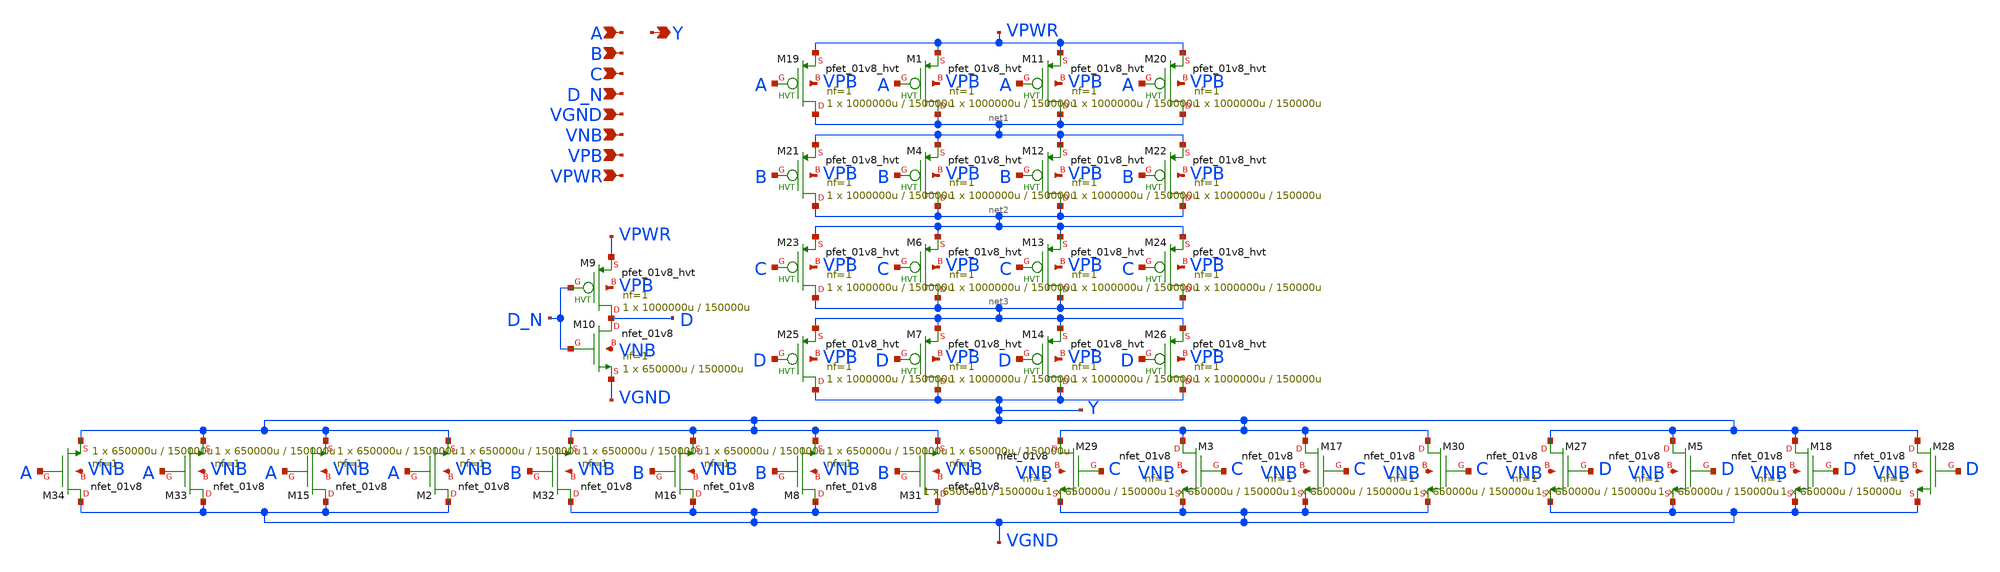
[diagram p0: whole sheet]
** sch_path: schematics/nor4b/sky130_fd_sc_hd__nor4b_4.sch
**.subckt sky130_fd_sc_hd__nor4b_4 A B C D_N VGND VNB VPB VPWR Y
*.ipin A
*.ipin B
*.ipin C
*.ipin D_N
*.ipin VGND
*.ipin VNB
*.ipin VPB
*.ipin VPWR
*.opin Y
XM1 net1 A VPWR VPB sky130_fd_pr__pfet_01v8_hvt L=150000u W=1000000u nf=1 ad='int((1 + 1)/2) * 1000000u / 1 * 0.29'
+ as='int((1 + 2)/2) * 1000000u / 1 * 0.29' pd='2*int((1 + 1)/2) * (1000000u / 1 + 0.29)' ps='2*int((1 + 2)/2) * (1000000u / 1 + 0.29)'
+ nrd='0.29 / 1000000u ' nrs='0.29 / 1000000u ' sa=0 sb=0 sd=0 mult=1 m=1
XM2 VGND A Y VNB sky130_fd_pr__nfet_01v8 L=150000u W=650000u nf=1 ad='int((1 + 1)/2) * 650000u / 1 * 0.29'
+ as='int((1 + 2)/2) * 650000u / 1 * 0.29' pd='2*int((1 + 1)/2) * (650000u / 1 + 0.29)' ps='2*int((1 + 2)/2) * (650000u / 1 + 0.29)'
+ nrd='0.29 / 650000u ' nrs='0.29 / 650000u ' sa=0 sb=0 sd=0 mult=1 m=1
XM4 net2 B net1 VPB sky130_fd_pr__pfet_01v8_hvt L=150000u W=1000000u nf=1 ad='int((1 + 1)/2) * 1000000u / 1 * 0.29'
+ as='int((1 + 2)/2) * 1000000u / 1 * 0.29' pd='2*int((1 + 1)/2) * (1000000u / 1 + 0.29)' ps='2*int((1 + 2)/2) * (1000000u / 1 + 0.29)'
+ nrd='0.29 / 1000000u ' nrs='0.29 / 1000000u ' sa=0 sb=0 sd=0 mult=1 m=1
XM3 Y C VGND VNB sky130_fd_pr__nfet_01v8 L=150000u W=650000u nf=1 ad='int((1 + 1)/2) * 650000u / 1 * 0.29'
+ as='int((1 + 2)/2) * 650000u / 1 * 0.29' pd='2*int((1 + 1)/2) * (650000u / 1 + 0.29)' ps='2*int((1 + 2)/2) * (650000u / 1 + 0.29)'
+ nrd='0.29 / 650000u ' nrs='0.29 / 650000u ' sa=0 sb=0 sd=0 mult=1 m=1
XM5 Y D VGND VNB sky130_fd_pr__nfet_01v8 L=150000u W=650000u nf=1 ad='int((1 + 1)/2) * 650000u / 1 * 0.29'
+ as='int((1 + 2)/2) * 650000u / 1 * 0.29' pd='2*int((1 + 1)/2) * (650000u / 1 + 0.29)' ps='2*int((1 + 2)/2) * (650000u / 1 + 0.29)'
+ nrd='0.29 / 650000u ' nrs='0.29 / 650000u ' sa=0 sb=0 sd=0 mult=1 m=1
XM6 net3 C net2 VPB sky130_fd_pr__pfet_01v8_hvt L=150000u W=1000000u nf=1 ad='int((1 + 1)/2) * 1000000u / 1 * 0.29'
+ as='int((1 + 2)/2) * 1000000u / 1 * 0.29' pd='2*int((1 + 1)/2) * (1000000u / 1 + 0.29)' ps='2*int((1 + 2)/2) * (1000000u / 1 + 0.29)'
+ nrd='0.29 / 1000000u ' nrs='0.29 / 1000000u ' sa=0 sb=0 sd=0 mult=1 m=1
XM7 Y D net3 VPB sky130_fd_pr__pfet_01v8_hvt L=150000u W=1000000u nf=1 ad='int((1 + 1)/2) * 1000000u / 1 * 0.29'
+ as='int((1 + 2)/2) * 1000000u / 1 * 0.29' pd='2*int((1 + 1)/2) * (1000000u / 1 + 0.29)' ps='2*int((1 + 2)/2) * (1000000u / 1 + 0.29)'
+ nrd='0.29 / 1000000u ' nrs='0.29 / 1000000u ' sa=0 sb=0 sd=0 mult=1 m=1
XM8 VGND B Y VNB sky130_fd_pr__nfet_01v8 L=150000u W=650000u nf=1 ad='int((1 + 1)/2) * 650000u / 1 * 0.29'
+ as='int((1 + 2)/2) * 650000u / 1 * 0.29' pd='2*int((1 + 1)/2) * (650000u / 1 + 0.29)' ps='2*int((1 + 2)/2) * (650000u / 1 + 0.29)'
+ nrd='0.29 / 650000u ' nrs='0.29 / 650000u ' sa=0 sb=0 sd=0 mult=1 m=1
XM9 D D_N VPWR VPB sky130_fd_pr__pfet_01v8_hvt L=150000u W=1000000u nf=1 ad='int((1 + 1)/2) * 1000000u / 1 * 0.29'
+ as='int((1 + 2)/2) * 1000000u / 1 * 0.29' pd='2*int((1 + 1)/2) * (1000000u / 1 + 0.29)' ps='2*int((1 + 2)/2) * (1000000u / 1 + 0.29)'
+ nrd='0.29 / 1000000u ' nrs='0.29 / 1000000u ' sa=0 sb=0 sd=0 mult=1 m=1
XM10 D D_N VGND VNB sky130_fd_pr__nfet_01v8 L=150000u W=650000u nf=1 ad='int((1 + 1)/2) * 650000u / 1 * 0.29'
+ as='int((1 + 2)/2) * 650000u / 1 * 0.29' pd='2*int((1 + 1)/2) * (650000u / 1 + 0.29)' ps='2*int((1 + 2)/2) * (650000u / 1 + 0.29)'
+ nrd='0.29 / 650000u ' nrs='0.29 / 650000u ' sa=0 sb=0 sd=0 mult=1 m=1
XM11 net1 A VPWR VPB sky130_fd_pr__pfet_01v8_hvt L=150000u W=1000000u nf=1 ad='int((1 + 1)/2) * 1000000u / 1 * 0.29'
+ as='int((1 + 2)/2) * 1000000u / 1 * 0.29' pd='2*int((1 + 1)/2) * (1000000u / 1 + 0.29)' ps='2*int((1 + 2)/2) * (1000000u / 1 + 0.29)'
+ nrd='0.29 / 1000000u ' nrs='0.29 / 1000000u ' sa=0 sb=0 sd=0 mult=1 m=1
XM12 net2 B net1 VPB sky130_fd_pr__pfet_01v8_hvt L=150000u W=1000000u nf=1 ad='int((1 + 1)/2) * 1000000u / 1 * 0.29'
+ as='int((1 + 2)/2) * 1000000u / 1 * 0.29' pd='2*int((1 + 1)/2) * (1000000u / 1 + 0.29)' ps='2*int((1 + 2)/2) * (1000000u / 1 + 0.29)'
+ nrd='0.29 / 1000000u ' nrs='0.29 / 1000000u ' sa=0 sb=0 sd=0 mult=1 m=1
XM13 net3 C net2 VPB sky130_fd_pr__pfet_01v8_hvt L=150000u W=1000000u nf=1 ad='int((1 + 1)/2) * 1000000u / 1 * 0.29'
+ as='int((1 + 2)/2) * 1000000u / 1 * 0.29' pd='2*int((1 + 1)/2) * (1000000u / 1 + 0.29)' ps='2*int((1 + 2)/2) * (1000000u / 1 + 0.29)'
+ nrd='0.29 / 1000000u ' nrs='0.29 / 1000000u ' sa=0 sb=0 sd=0 mult=1 m=1
XM14 Y D net3 VPB sky130_fd_pr__pfet_01v8_hvt L=150000u W=1000000u nf=1 ad='int((1 + 1)/2) * 1000000u / 1 * 0.29'
+ as='int((1 + 2)/2) * 1000000u / 1 * 0.29' pd='2*int((1 + 1)/2) * (1000000u / 1 + 0.29)' ps='2*int((1 + 2)/2) * (1000000u / 1 + 0.29)'
+ nrd='0.29 / 1000000u ' nrs='0.29 / 1000000u ' sa=0 sb=0 sd=0 mult=1 m=1
XM15 VGND A Y VNB sky130_fd_pr__nfet_01v8 L=150000u W=650000u nf=1 ad='int((1 + 1)/2) * 650000u / 1 * 0.29'
+ as='int((1 + 2)/2) * 650000u / 1 * 0.29' pd='2*int((1 + 1)/2) * (650000u / 1 + 0.29)' ps='2*int((1 + 2)/2) * (650000u / 1 + 0.29)'
+ nrd='0.29 / 650000u ' nrs='0.29 / 650000u ' sa=0 sb=0 sd=0 mult=1 m=1
XM16 VGND B Y VNB sky130_fd_pr__nfet_01v8 L=150000u W=650000u nf=1 ad='int((1 + 1)/2) * 650000u / 1 * 0.29'
+ as='int((1 + 2)/2) * 650000u / 1 * 0.29' pd='2*int((1 + 1)/2) * (650000u / 1 + 0.29)' ps='2*int((1 + 2)/2) * (650000u / 1 + 0.29)'
+ nrd='0.29 / 650000u ' nrs='0.29 / 650000u ' sa=0 sb=0 sd=0 mult=1 m=1
XM17 Y C VGND VNB sky130_fd_pr__nfet_01v8 L=150000u W=650000u nf=1 ad='int((1 + 1)/2) * 650000u / 1 * 0.29'
+ as='int((1 + 2)/2) * 650000u / 1 * 0.29' pd='2*int((1 + 1)/2) * (650000u / 1 + 0.29)' ps='2*int((1 + 2)/2) * (650000u / 1 + 0.29)'
+ nrd='0.29 / 650000u ' nrs='0.29 / 650000u ' sa=0 sb=0 sd=0 mult=1 m=1
XM18 Y D VGND VNB sky130_fd_pr__nfet_01v8 L=150000u W=650000u nf=1 ad='int((1 + 1)/2) * 650000u / 1 * 0.29'
+ as='int((1 + 2)/2) * 650000u / 1 * 0.29' pd='2*int((1 + 1)/2) * (650000u / 1 + 0.29)' ps='2*int((1 + 2)/2) * (650000u / 1 + 0.29)'
+ nrd='0.29 / 650000u ' nrs='0.29 / 650000u ' sa=0 sb=0 sd=0 mult=1 m=1
XM19 net1 A VPWR VPB sky130_fd_pr__pfet_01v8_hvt L=150000u W=1000000u nf=1 ad='int((1 + 1)/2) * 1000000u / 1 * 0.29'
+ as='int((1 + 2)/2) * 1000000u / 1 * 0.29' pd='2*int((1 + 1)/2) * (1000000u / 1 + 0.29)' ps='2*int((1 + 2)/2) * (1000000u / 1 + 0.29)'
+ nrd='0.29 / 1000000u ' nrs='0.29 / 1000000u ' sa=0 sb=0 sd=0 mult=1 m=1
XM20 net1 A VPWR VPB sky130_fd_pr__pfet_01v8_hvt L=150000u W=1000000u nf=1 ad='int((1 + 1)/2) * 1000000u / 1 * 0.29'
+ as='int((1 + 2)/2) * 1000000u / 1 * 0.29' pd='2*int((1 + 1)/2) * (1000000u / 1 + 0.29)' ps='2*int((1 + 2)/2) * (1000000u / 1 + 0.29)'
+ nrd='0.29 / 1000000u ' nrs='0.29 / 1000000u ' sa=0 sb=0 sd=0 mult=1 m=1
XM21 net2 B net1 VPB sky130_fd_pr__pfet_01v8_hvt L=150000u W=1000000u nf=1 ad='int((1 + 1)/2) * 1000000u / 1 * 0.29'
+ as='int((1 + 2)/2) * 1000000u / 1 * 0.29' pd='2*int((1 + 1)/2) * (1000000u / 1 + 0.29)' ps='2*int((1 + 2)/2) * (1000000u / 1 + 0.29)'
+ nrd='0.29 / 1000000u ' nrs='0.29 / 1000000u ' sa=0 sb=0 sd=0 mult=1 m=1
XM22 net2 B net1 VPB sky130_fd_pr__pfet_01v8_hvt L=150000u W=1000000u nf=1 ad='int((1 + 1)/2) * 1000000u / 1 * 0.29'
+ as='int((1 + 2)/2) * 1000000u / 1 * 0.29' pd='2*int((1 + 1)/2) * (1000000u / 1 + 0.29)' ps='2*int((1 + 2)/2) * (1000000u / 1 + 0.29)'
+ nrd='0.29 / 1000000u ' nrs='0.29 / 1000000u ' sa=0 sb=0 sd=0 mult=1 m=1
XM23 net3 C net2 VPB sky130_fd_pr__pfet_01v8_hvt L=150000u W=1000000u nf=1 ad='int((1 + 1)/2) * 1000000u / 1 * 0.29'
+ as='int((1 + 2)/2) * 1000000u / 1 * 0.29' pd='2*int((1 + 1)/2) * (1000000u / 1 + 0.29)' ps='2*int((1 + 2)/2) * (1000000u / 1 + 0.29)'
+ nrd='0.29 / 1000000u ' nrs='0.29 / 1000000u ' sa=0 sb=0 sd=0 mult=1 m=1
XM24 net3 C net2 VPB sky130_fd_pr__pfet_01v8_hvt L=150000u W=1000000u nf=1 ad='int((1 + 1)/2) * 1000000u / 1 * 0.29'
+ as='int((1 + 2)/2) * 1000000u / 1 * 0.29' pd='2*int((1 + 1)/2) * (1000000u / 1 + 0.29)' ps='2*int((1 + 2)/2) * (1000000u / 1 + 0.29)'
+ nrd='0.29 / 1000000u ' nrs='0.29 / 1000000u ' sa=0 sb=0 sd=0 mult=1 m=1
XM25 Y D net3 VPB sky130_fd_pr__pfet_01v8_hvt L=150000u W=1000000u nf=1 ad='int((1 + 1)/2) * 1000000u / 1 * 0.29'
+ as='int((1 + 2)/2) * 1000000u / 1 * 0.29' pd='2*int((1 + 1)/2) * (1000000u / 1 + 0.29)' ps='2*int((1 + 2)/2) * (1000000u / 1 + 0.29)'
+ nrd='0.29 / 1000000u ' nrs='0.29 / 1000000u ' sa=0 sb=0 sd=0 mult=1 m=1
XM26 Y D net3 VPB sky130_fd_pr__pfet_01v8_hvt L=150000u W=1000000u nf=1 ad='int((1 + 1)/2) * 1000000u / 1 * 0.29'
+ as='int((1 + 2)/2) * 1000000u / 1 * 0.29' pd='2*int((1 + 1)/2) * (1000000u / 1 + 0.29)' ps='2*int((1 + 2)/2) * (1000000u / 1 + 0.29)'
+ nrd='0.29 / 1000000u ' nrs='0.29 / 1000000u ' sa=0 sb=0 sd=0 mult=1 m=1
XM27 Y D VGND VNB sky130_fd_pr__nfet_01v8 L=150000u W=650000u nf=1 ad='int((1 + 1)/2) * 650000u / 1 * 0.29'
+ as='int((1 + 2)/2) * 650000u / 1 * 0.29' pd='2*int((1 + 1)/2) * (650000u / 1 + 0.29)' ps='2*int((1 + 2)/2) * (650000u / 1 + 0.29)'
+ nrd='0.29 / 650000u ' nrs='0.29 / 650000u ' sa=0 sb=0 sd=0 mult=1 m=1
XM28 Y D VGND VNB sky130_fd_pr__nfet_01v8 L=150000u W=650000u nf=1 ad='int((1 + 1)/2) * 650000u / 1 * 0.29'
+ as='int((1 + 2)/2) * 650000u / 1 * 0.29' pd='2*int((1 + 1)/2) * (650000u / 1 + 0.29)' ps='2*int((1 + 2)/2) * (650000u / 1 + 0.29)'
+ nrd='0.29 / 650000u ' nrs='0.29 / 650000u ' sa=0 sb=0 sd=0 mult=1 m=1
XM29 Y C VGND VNB sky130_fd_pr__nfet_01v8 L=150000u W=650000u nf=1 ad='int((1 + 1)/2) * 650000u / 1 * 0.29'
+ as='int((1 + 2)/2) * 650000u / 1 * 0.29' pd='2*int((1 + 1)/2) * (650000u / 1 + 0.29)' ps='2*int((1 + 2)/2) * (650000u / 1 + 0.29)'
+ nrd='0.29 / 650000u ' nrs='0.29 / 650000u ' sa=0 sb=0 sd=0 mult=1 m=1
XM30 Y C VGND VNB sky130_fd_pr__nfet_01v8 L=150000u W=650000u nf=1 ad='int((1 + 1)/2) * 650000u / 1 * 0.29'
+ as='int((1 + 2)/2) * 650000u / 1 * 0.29' pd='2*int((1 + 1)/2) * (650000u / 1 + 0.29)' ps='2*int((1 + 2)/2) * (650000u / 1 + 0.29)'
+ nrd='0.29 / 650000u ' nrs='0.29 / 650000u ' sa=0 sb=0 sd=0 mult=1 m=1
XM31 VGND B Y VNB sky130_fd_pr__nfet_01v8 L=150000u W=650000u nf=1 ad='int((1 + 1)/2) * 650000u / 1 * 0.29'
+ as='int((1 + 2)/2) * 650000u / 1 * 0.29' pd='2*int((1 + 1)/2) * (650000u / 1 + 0.29)' ps='2*int((1 + 2)/2) * (650000u / 1 + 0.29)'
+ nrd='0.29 / 650000u ' nrs='0.29 / 650000u ' sa=0 sb=0 sd=0 mult=1 m=1
XM32 VGND B Y VNB sky130_fd_pr__nfet_01v8 L=150000u W=650000u nf=1 ad='int((1 + 1)/2) * 650000u / 1 * 0.29'
+ as='int((1 + 2)/2) * 650000u / 1 * 0.29' pd='2*int((1 + 1)/2) * (650000u / 1 + 0.29)' ps='2*int((1 + 2)/2) * (650000u / 1 + 0.29)'
+ nrd='0.29 / 650000u ' nrs='0.29 / 650000u ' sa=0 sb=0 sd=0 mult=1 m=1
XM33 VGND A Y VNB sky130_fd_pr__nfet_01v8 L=150000u W=650000u nf=1 ad='int((1 + 1)/2) * 650000u / 1 * 0.29'
+ as='int((1 + 2)/2) * 650000u / 1 * 0.29' pd='2*int((1 + 1)/2) * (650000u / 1 + 0.29)' ps='2*int((1 + 2)/2) * (650000u / 1 + 0.29)'
+ nrd='0.29 / 650000u ' nrs='0.29 / 650000u ' sa=0 sb=0 sd=0 mult=1 m=1
XM34 VGND A Y VNB sky130_fd_pr__nfet_01v8 L=150000u W=650000u nf=1 ad='int((1 + 1)/2) * 650000u / 1 * 0.29'
+ as='int((1 + 2)/2) * 650000u / 1 * 0.29' pd='2*int((1 + 1)/2) * (650000u / 1 + 0.29)' ps='2*int((1 + 2)/2) * (650000u / 1 + 0.29)'
+ nrd='0.29 / 650000u ' nrs='0.29 / 650000u ' sa=0 sb=0 sd=0 mult=1 m=1
**.ends
.end
